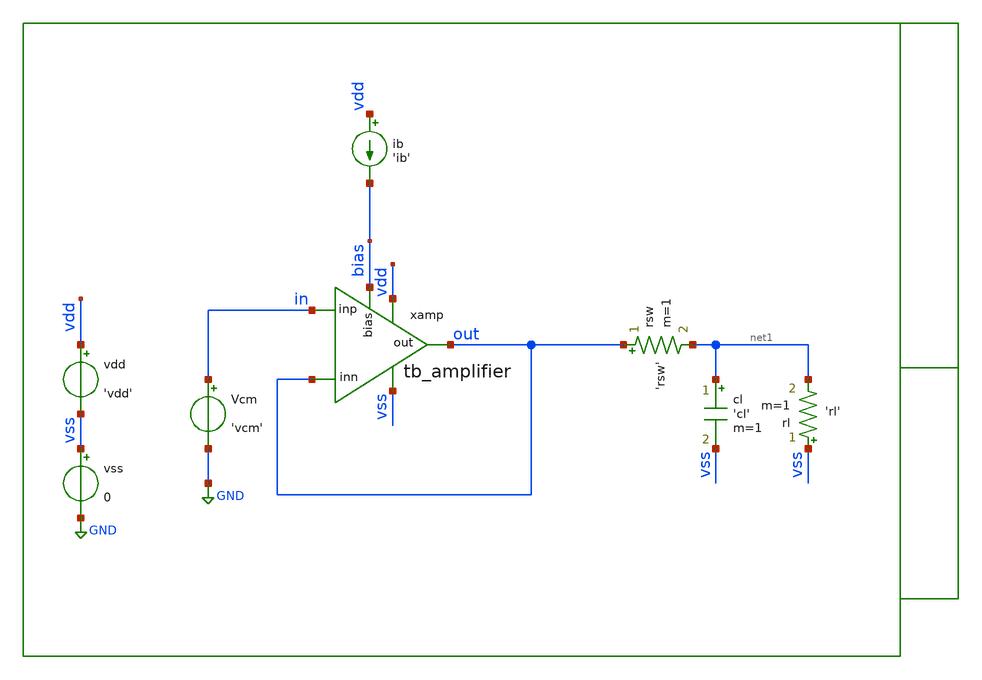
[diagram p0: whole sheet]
** sch_path: xschem/tb/testbuffer/tb_amplifier/op_tb_amplifier.sch
**.subckt op_tb_amplifier
ib vdd bias 'ib'
xamp vdd out in out vss bias tb_amplifier
Vcm in GND 'vcm'
vdd vdd vss 'vdd'
vss vss GND 0
cl net1 vss 'cl' m=1
rl vss net1 'rl' m=1
rsw out net1 'rsw' m=1
**** begin user architecture code

* Control

.param vdd=3.3
.param vcm='vdd/2'
.param ib=5u
.param cl=10p
.param rl=1e6
.param rsw=1

.control
save all
op

let l_xm4 = @m.xamp.xm4.m0[l]
let l_xm5 = @m.xamp.xm5.m0[l]
let l_xm6 = @m.xamp.xm6.m0[l]
let l_xm7 = @m.xamp.xm7.m0[l]
let m_xm4 = @m.xamp.xm4.m0[m]
let m_xm5 = @m.xamp.xm5.m0[m]
let m_xm6 = @m.xamp.xm6.m0[m]
let m_xm7 = @m.xamp.xm7.m0[m]
let w_xm4 = @m.xamp.xm4.m0[w]
let w_xm5 = @m.xamp.xm5.m0[w]
let w_xm6 = @m.xamp.xm6.m0[w]
let w_xm7 = @m.xamp.xm7.m0[w]

let s4 = m_xm4*w_xm4/l_xm4
let s5 = m_xm5*w_xm5/l_xm5
let s6 = m_xm6*w_xm6/l_xm6
let s7 = m_xm7*w_xm7/l_xm7

let gm_xm4 = @m.xamp.xm4.m0[gm]
let gm_xmb1 = @m.xamp.xmb1.m0[gm]
let gm_xm5 = @m.xamp.xm5.m0[gm]
let gm_xm6 = @m.xamp.xm6.m0[gm]
let gm_xm1 = @m.xamp.xm1.m0[gm]
let gm_xm2 = @m.xamp.xm2.m0[gm]
let gm_xm3 = @m.xamp.xm3.m0[gm]
let gm_xm7 = @m.xamp.xm7.m0[gm]
let gm_xmb2 = @m.xamp.xmb2.m0[gm]
let gm_xmb3 = @m.xamp.xmb3.m0[gm]
let gm_xmb4 = @m.xamp.xmb4.m0[gm]
let gds_xm4 = @m.xamp.xm4.m0[gds]
let gds_xmb1 = @m.xamp.xmb1.m0[gds]
let gds_xm5 = @m.xamp.xm5.m0[gds]
let gds_xm6 = @m.xamp.xm6.m0[gds]
let gds_xm1 = @m.xamp.xm1.m0[gds]
let gds_xm2 = @m.xamp.xm2.m0[gds]
let gds_xm3 = @m.xamp.xm3.m0[gds]
let gds_xm7 = @m.xamp.xm7.m0[gds]
let gds_xmb2 = @m.xamp.xmb2.m0[gds]
let gds_xmb3 = @m.xamp.xmb3.m0[gds]
let gds_xmb4 = @m.xamp.xmb4.m0[gds]
let vdsat_xm4 = @m.xamp.xm4.m0[vdsat]
let vdsat_xmb1 = @m.xamp.xmb1.m0[vdsat]
let vdsat_xm5 = @m.xamp.xm5.m0[vdsat]
let vdsat_xm6 = @m.xamp.xm6.m0[vdsat]
let vdsat_xm1 = @m.xamp.xm1.m0[vdsat]
let vdsat_xm2 = @m.xamp.xm2.m0[vdsat]
let vdsat_xm3 = @m.xamp.xm3.m0[vdsat]
let vdsat_xm7 = @m.xamp.xm7.m0[vdsat]
let vdsat_xmb2 = @m.xamp.xmb2.m0[vdsat]
let vdsat_xmb3 = @m.xamp.xmb3.m0[vdsat]
let vdsat_xmb4 = @m.xamp.xmb4.m0[vdsat]
let vth_xm4 = @m.xamp.xm4.m0[vth]
let vth_xmb1 = @m.xamp.xmb1.m0[vth]
let vth_xm5 = @m.xamp.xm5.m0[vth]
let vth_xm6 = @m.xamp.xm6.m0[vth]
let vth_xm1 = @m.xamp.xm1.m0[vth]
let vth_xm2 = @m.xamp.xm2.m0[vth]
let vth_xm3 = @m.xamp.xm3.m0[vth]
let vth_xm7 = @m.xamp.xm7.m0[vth]
let vth_xmb2 = @m.xamp.xmb2.m0[vth]
let vth_xmb3 = @m.xamp.xmb3.m0[vth]
let vth_xmb4 = @m.xamp.xmb4.m0[vth]
let id_xm4 = @m.xamp.xm4.m0[id]
let id_xmb1 = @m.xamp.xmb1.m0[id]
let id_xm5 = @m.xamp.xm5.m0[id]
let id_xm6 = @m.xamp.xm6.m0[id]
let id_xm1 = @m.xamp.xm1.m0[id]
let id_xm2 = @m.xamp.xm2.m0[id]
let id_xm3 = @m.xamp.xm3.m0[id]
let id_xm7 = @m.xamp.xm7.m0[id]
let id_xmb2 = @m.xamp.xmb2.m0[id]
let id_xmb3 = @m.xamp.xmb3.m0[id]
let id_xmb4 = @m.xamp.xmb4.m0[id]
let vgs_xm4 = @m.xamp.xm4.m0[vgs]
let vgs_xmb1 = @m.xamp.xmb1.m0[vgs]
let vgs_xm5 = @m.xamp.xm5.m0[vgs]
let vgs_xm6 = @m.xamp.xm6.m0[vgs]
let vgs_xm1 = @m.xamp.xm1.m0[vgs]
let vgs_xm2 = @m.xamp.xm2.m0[vgs]
let vgs_xm3 = @m.xamp.xm3.m0[vgs]
let vgs_xm7 = @m.xamp.xm7.m0[vgs]
let vgs_xmb2 = @m.xamp.xmb2.m0[vgs]
let vgs_xmb3 = @m.xamp.xmb3.m0[vgs]
let vgs_xmb4 = @m.xamp.xmb4.m0[vgs]
let vds_xm4 = @m.xamp.xm4.m0[vds]
let vds_xmb1 = @m.xamp.xmb1.m0[vds]
let vds_xm5 = @m.xamp.xm5.m0[vds]
let vds_xm6 = @m.xamp.xm6.m0[vds]
let vds_xm1 = @m.xamp.xm1.m0[vds]
let vds_xm2 = @m.xamp.xm2.m0[vds]
let vds_xm3 = @m.xamp.xm3.m0[vds]
let vds_xm7 = @m.xamp.xm7.m0[vds]
let vds_xmb2 = @m.xamp.xmb2.m0[vds]
let vds_xmb3 = @m.xamp.xmb3.m0[vds]
let vds_xmb4 = @m.xamp.xmb4.m0[vds]

let vsat_xm4 = vds_xm4 - vdsat_xm4
let vsat_xmb1 = vds_xmb1 - vdsat_xmb1
let vsat_xm5 = vds_xm5 - vdsat_xm5
let vsat_xm6 = vds_xm6 - vdsat_xm6
let vsat_xm1 = vds_xm1 - vdsat_xm1
let vsat_xm2 = vds_xm2 - vdsat_xm2
let vsat_xm3 = vds_xm3 - vdsat_xm3
let vsat_xm7 = vds_xm7 - vdsat_xm7
let vsat_xmb2 = vds_xmb2 - vdsat_xmb2
let vsat_xmb3 = vds_xmb3 - vdsat_xmb3
let vsat_xmb4 = vds_xmb4 - vdsat_xmb4

let vov_xm4 = vgs_xm4 - vth_xm4
let vov_xmb1 = vgs_xmb1 - vth_xmb1
let vov_xm5 = vgs_xm5 - vth_xm5
let vov_xm6 = vgs_xm6 - vth_xm6
let vov_xm1 = vgs_xm1 - vth_xm1
let vov_xm2 = vgs_xm2 - vth_xm2
let vov_xm3 = vgs_xm3 - vth_xm3
let vov_xm7 = vgs_xm7 - vth_xm7
let vov_xmb2 = vgs_xmb2 - vth_xmb2
let vov_xmb3 = vgs_xmb3 - vth_xmb3
let vov_xmb4 = vgs_xmb4 - vth_xmb4


let voff = in - out
let voff_rhs = (s7/s4)
let voff_lhs = 2*(s6/s5)

let comp = xamp.comp
let vbm  = xamp.vbm
let vbt  = xamp.vbt
let mirr = xamp.mirr
let vcm  = xamp.vcm



print gm_xm4
print gm_xmb1
print gm_xm5
print gm_xm6
print gm_xm1
print gm_xm2
print gm_xm3
print gm_xm7
print gm_xmb2
print gm_xmb3
print gm_xmb4
print gds_xm1
print gds_xm2
print gds_xm4
print gds_xmb1
print gds_xm5
print gds_xm6
print gds_xm1
print gds_xm2
print gds_xm3
print gds_xm7
print gds_xmb2
print gds_xmb3
print gds_xmb4
print vdsat_xm1
print vdsat_xm2
print vdsat_xm4
print vdsat_xmb1
print vdsat_xm5
print vdsat_xm6
print vdsat_xm1
print vdsat_xm2
print vdsat_xm3
print vdsat_xm7
print vdsat_xmb2
print vdsat_xmb3
print vdsat_xmb4
print vth_xm1
print vth_xm2
print vth_xm4
print vth_xmb1
print vth_xm5
print vth_xm6
print vth_xm1
print vth_xm2
print vth_xm3
print vth_xm7
print vth_xmb2
print vth_xmb3
print vth_xmb4
print id_xm1
print id_xm2
print id_xm4
print id_xmb1
print id_xm5
print id_xm6
print id_xm1
print id_xm2
print id_xm3
print id_xm7
print id_xmb2
print id_xmb3
print id_xmb4
print vgs_xm1
print vgs_xm2
print vgs_xm4
print vgs_xmb1
print vgs_xm5
print vgs_xm6
print vgs_xm1
print vgs_xm2
print vgs_xm3
print vgs_xm7
print vgs_xmb2
print vgs_xmb3
print vgs_xmb4
print vds_xm1
print vds_xm2
print vds_xm4
print vds_xmb1
print vds_xm5
print vds_xm6
print vds_xm1
print vds_xm2
print vds_xm3
print vds_xm7
print vds_xmb2
print vds_xmb3
print vds_xmb4
print vsat_xm1
print vsat_xm2
print vsat_xm4
print vsat_xmb1
print vsat_xm5
print vsat_xm6
print vsat_xm1
print vsat_xm2
print vsat_xm3
print vsat_xm7
print vsat_xmb2
print vsat_xmb3
print vsat_xmb4

print vov_xm1
print vov_xm2
print vov_xm4
print vov_xmb1
print vov_xm5
print vov_xm6
print vov_xm1
print vov_xm2
print vov_xm3
print vov_xm7
print vov_xmb2
print vov_xmb3
print vov_xmb4

print comp
print vbm
print vbt
print mirr
print vcm
print bias
print in
print out

print voff
print voff_rhs
print voff_lhs



write op_tb_amplifier.raw

.endc


 * Model Corners

.include $::CORNERS/ngspice/tt.spice
*.include $::CORNERS/ngspice/ff.spice
*.include $::CORNERS/ngspice/ss.spice
*.include $::CORNERS/ngspice/sf.spice
*.include $::CORNERS/ngspice/fs.spice

**** end user architecture code
**.ends

* expanding   symbol:  sch/testbuffer/tb_amplifier/tb_amplifier.sym # of pins=6
** sym_path: xschem/sch/testbuffer/tb_amplifier/tb_amplifier.sym
** sch_path: xschem/sch/testbuffer/tb_amplifier/tb_amplifier.sch
.subckt tb_amplifier vdd out inp inn vss bias
*.ipin inn
*.ipin inp
*.opin out
*.iopin bias
*.iopin vdd
*.iopin vss
XM3 mirr mirr vdd vdd pfet_06v0 L=4u W=16u nf=2 ad='int((nf+1)/2) * W/nf * 0.18u' as='int((nf+2)/2) * W/nf * 0.18u'
+ pd='2*int((nf+1)/2) * (W/nf + 0.18u)' ps='2*int((nf+2)/2) * (W/nf + 0.18u)' nrd='0.18u / W' nrs='0.18u / W'
+ sa=0 sb=0 sd=0 m=2 par=2
XM4 comp mirr vdd vdd pfet_06v0 L=4u W=16u nf=2 ad='int((nf+1)/2) * W/nf * 0.18u' as='int((nf+2)/2) * W/nf * 0.18u'
+ pd='2*int((nf+1)/2) * (W/nf + 0.18u)' ps='2*int((nf+2)/2) * (W/nf + 0.18u)' nrd='0.18u / W' nrs='0.18u / W'
+ sa=0 sb=0 sd=0 m=2 par=2
XM2 comp inp vcm vss nfet_06v0 L=2u W=16u nf=2 ad='int((nf+1)/2) * W/nf * 0.18u' as='int((nf+2)/2) * W/nf * 0.18u'
+ pd='2*int((nf+1)/2) * (W/nf + 0.18u)' ps='2*int((nf+2)/2) * (W/nf + 0.18u)' nrd='0.18u / W' nrs='0.18u / W'
+ sa=0 sb=0 sd=0 m=2 par=2
XM1 mirr inn vcm vss nfet_06v0 L=2u W=16u nf=2 ad='int((nf+1)/2) * W/nf * 0.18u' as='int((nf+2)/2) * W/nf * 0.18u'
+ pd='2*int((nf+1)/2) * (W/nf + 0.18u)' ps='2*int((nf+2)/2) * (W/nf + 0.18u)' nrd='0.18u / W' nrs='0.18u / W'
+ sa=0 sb=0 sd=0 m=2 par=2
XM5 vcm bias vss vss nfet_06v0 L=1u W=16u nf=2 ad='int((nf+1)/2) * W/nf * 0.18u' as='int((nf+2)/2) * W/nf * 0.18u'
+ pd='2*int((nf+1)/2) * (W/nf + 0.18u)' ps='2*int((nf+2)/2) * (W/nf + 0.18u)' nrd='0.18u / W' nrs='0.18u / W'
+ sa=0 sb=0 sd=0 m=2 par=2
XM6 out bias vss vss nfet_06v0 L=1u W=16u nf=2 ad='int((nf+1)/2) * W/nf * 0.18u' as='int((nf+2)/2) * W/nf * 0.18u'
+ pd='2*int((nf+1)/2) * (W/nf + 0.18u)' ps='2*int((nf+2)/2) * (W/nf + 0.18u)' nrd='0.18u / W' nrs='0.18u / W'
+ sa=0 sb=0 sd=0 m=12 par=12
XM7 out comp vdd vdd pfet_06v0 L=1u W=96u nf=12 ad='int((nf+1)/2) * W/nf * 0.18u' as='int((nf+2)/2) * W/nf * 0.18u'
+ pd='2*int((nf+1)/2) * (W/nf + 0.18u)' ps='2*int((nf+2)/2) * (W/nf + 0.18u)' nrd='0.18u / W' nrs='0.18u / W'
+ sa=0 sb=0 sd=0 m=1 par=1
XMB1 bias bias vss vss nfet_06v0 L=1u W=16u nf=2 ad='int((nf+1)/2) * W/nf * 0.18u' as='int((nf+2)/2) * W/nf * 0.18u'
+ pd='2*int((nf+1)/2) * (W/nf + 0.18u)' ps='2*int((nf+2)/2) * (W/nf + 0.18u)' nrd='0.18u / W' nrs='0.18u / W'
+ sa=0 sb=0 sd=0 m=2 par=2
XMB2 vbm bias vss vss nfet_06v0 L=1u W=16u nf=2 ad='int((nf+1)/2) * W/nf * 0.18u' as='int((nf+2)/2) * W/nf * 0.18u'
+ pd='2*int((nf+1)/2) * (W/nf + 0.18u)' ps='2*int((nf+2)/2) * (W/nf + 0.18u)' nrd='0.18u / W' nrs='0.18u / W'
+ sa=0 sb=0 sd=0 m=2 par=2
XMB3 vbm vbm vbt vdd pfet_06v0 L=1u W=16u nf=2 ad='int((nf+1)/2) * W/nf * 0.18u' as='int((nf+2)/2) * W/nf * 0.18u'
+ pd='2*int((nf+1)/2) * (W/nf + 0.18u)' ps='2*int((nf+2)/2) * (W/nf + 0.18u)' nrd='0.18u / W' nrs='0.18u / W'
+ sa=0 sb=0 sd=0 m=1 par=1
XMB4 vbt vbt vdd vdd pfet_06v0 L=1u W=16u nf=2 ad='int((nf+1)/2) * W/nf * 0.18u' as='int((nf+2)/2) * W/nf * 0.18u'
+ pd='2*int((nf+1)/2) * (W/nf + 0.18u)' ps='2*int((nf+2)/2) * (W/nf + 0.18u)' nrd='0.18u / W' nrs='0.18u / W'
+ sa=0 sb=0 sd=0 m=1 par=1
XRCC gc comp vdd ppolyf_u_1k_6p0 r_width=2e-6 r_length=38e-6 s=1 m=1
XMDUM1 vss vss vss vss nfet_06v0 L=2u W=16u nf=2 ad='int((nf+1)/2) * W/nf * 0.18u' as='int((nf+2)/2) * W/nf * 0.18u'
+ pd='2*int((nf+1)/2) * (W/nf + 0.18u)' ps='2*int((nf+2)/2) * (W/nf + 0.18u)' nrd='0.18u / W' nrs='0.18u / W'
+ sa=0 sb=0 sd=0 m=2 par=2
XMDUM2 vdd vdd vdd vdd pfet_06v0 L=4u W=16u nf=2 ad='int((nf+1)/2) * W/nf * 0.18u' as='int((nf+2)/2) * W/nf * 0.18u'
+ pd='2*int((nf+1)/2) * (W/nf + 0.18u)' ps='2*int((nf+2)/2) * (W/nf + 0.18u)' nrd='0.18u / W' nrs='0.18u / W'
+ sa=0 sb=0 sd=0 m=4 par=4
XC1 out gc cap_mim_2f0_m4m5_noshield c_width=30e-6 c_length=30e-6 m=1
.ends

.GLOBAL GND
.end
